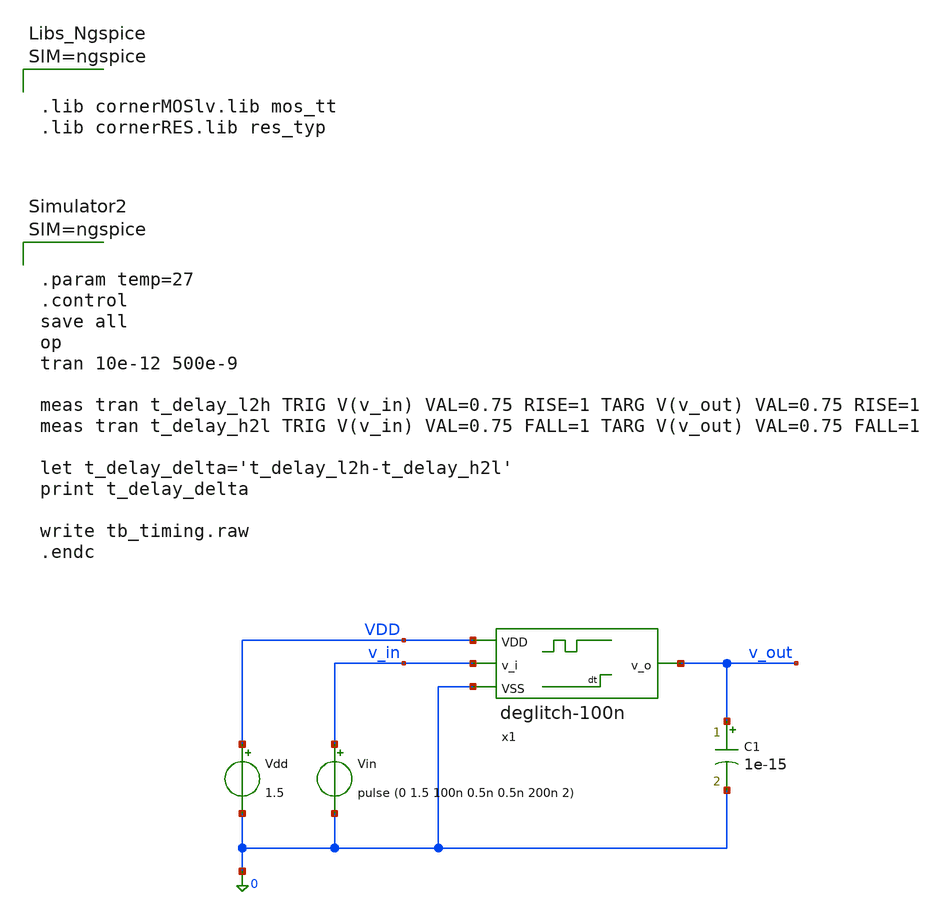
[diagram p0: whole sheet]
** sch_path: tb_timing.sch
**.subckt tb_timing
Vdd VDD 0 1.5
Vin v_in 0 pulse (0 1.5 100n 0.5n 0.5n 200n 2)
C1 v_out 0 1e-15 m=1
x1 VDD v_in v_out 0 deglitch-100n
**** begin user architecture code



.lib cornerMOSlv.lib mos_tt
.lib cornerRES.lib res_typ






.param temp=27
.control
save all
op
tran 10e-12 500e-9

meas tran t_delay_l2h TRIG V(v_in) VAL=0.75 RISE=1 TARG V(v_out) VAL=0.75 RISE=1
meas tran t_delay_h2l TRIG V(v_in) VAL=0.75 FALL=1 TARG V(v_out) VAL=0.75 FALL=1

let t_delay_delta='t_delay_l2h-t_delay_h2l'
print t_delay_delta

write tb_timing.raw
.endc



**** end user architecture code
**.ends
.end
